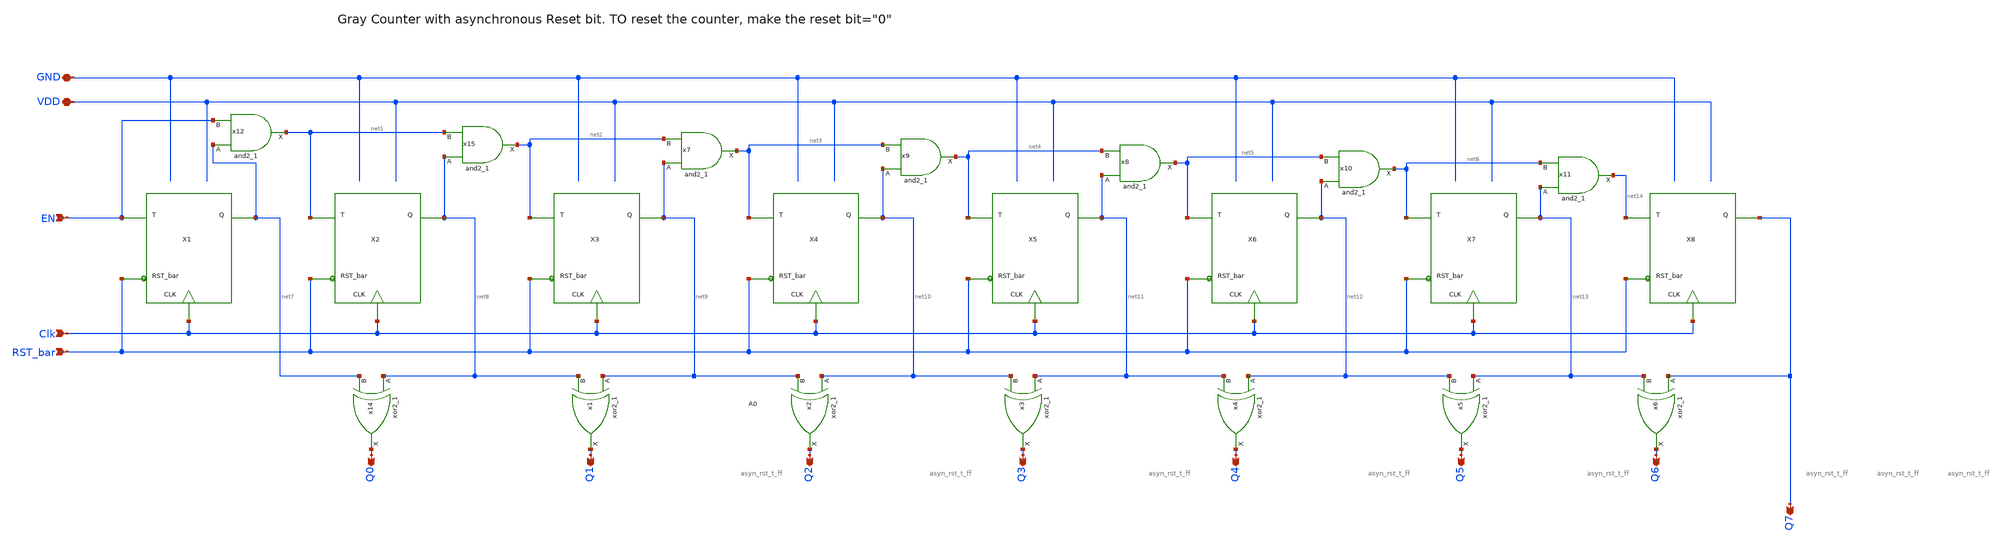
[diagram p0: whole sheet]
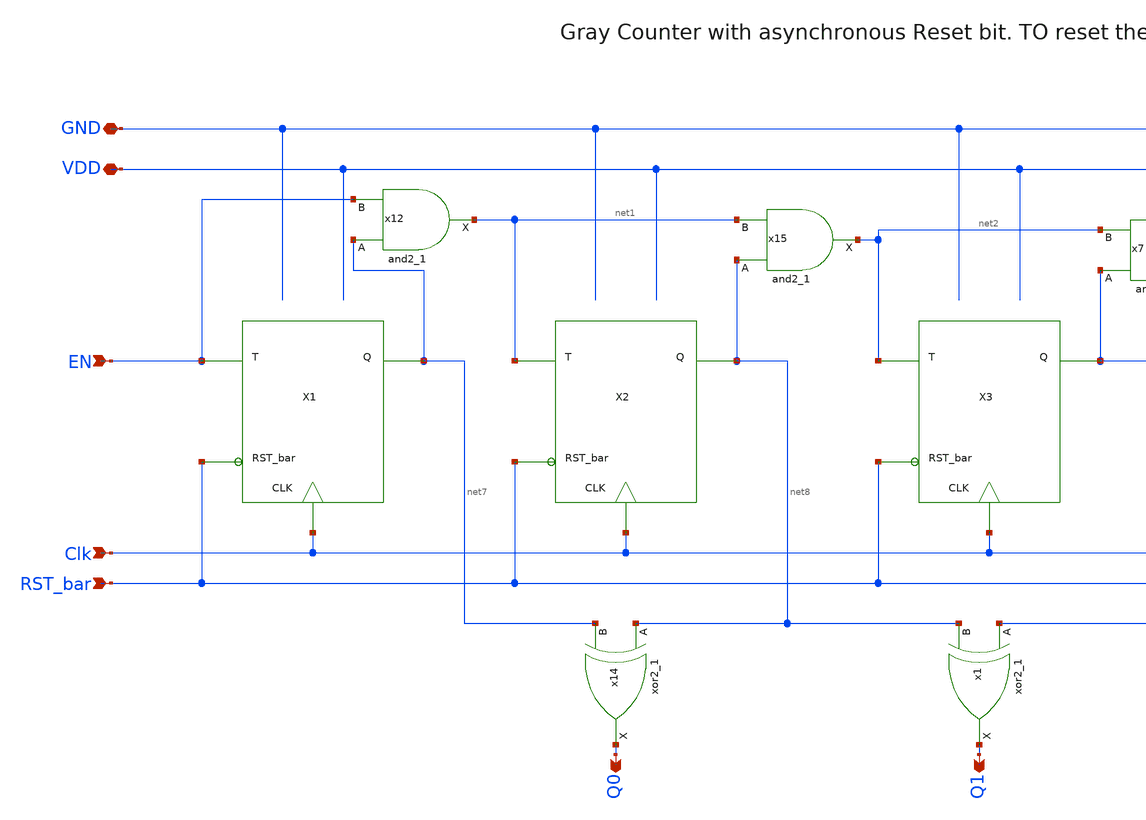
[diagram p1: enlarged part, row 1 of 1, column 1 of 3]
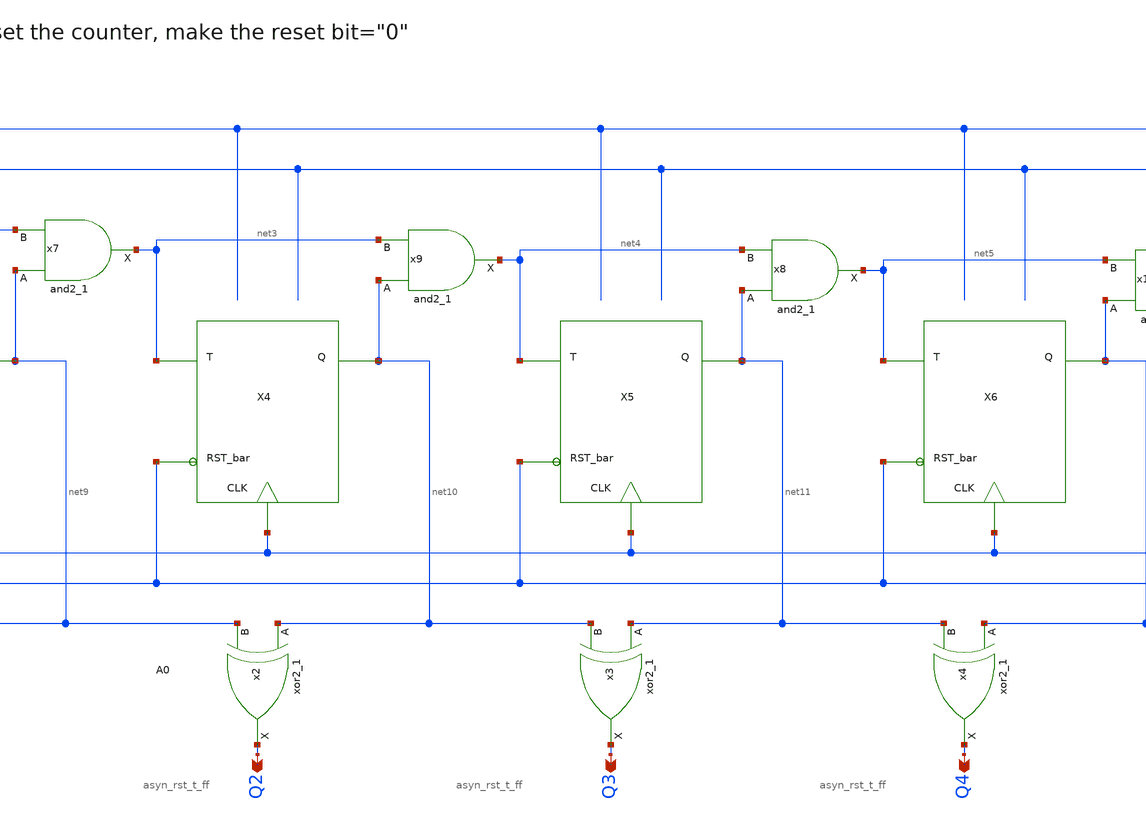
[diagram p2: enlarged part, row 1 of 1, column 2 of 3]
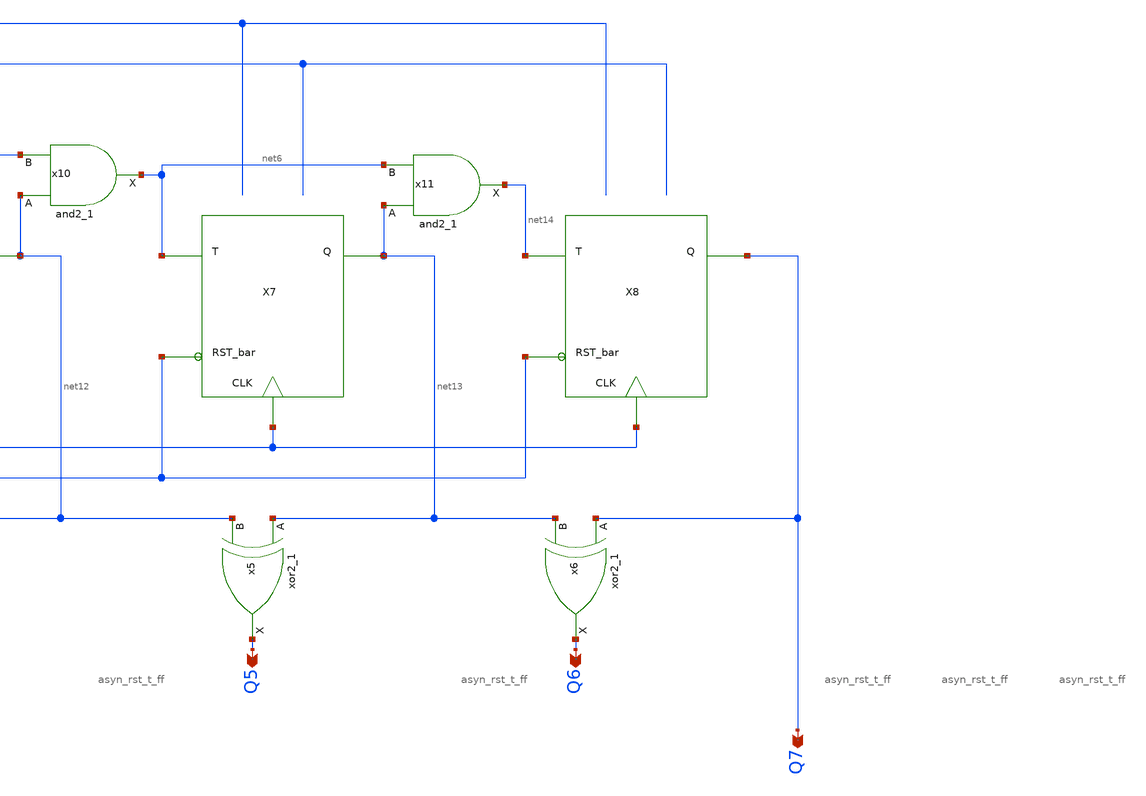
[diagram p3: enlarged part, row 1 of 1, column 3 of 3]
** sch_path: xschem/Asyn_rst_gray_counter/asyn_rst_gray_counter.sch
**.subckt asyn_rst_gray_counter Clk EN Q0 Q1 Q2 Q4 Q5 Q6 Q7 Q3 RST_bar VDD GND
*.ipin Clk
*.ipin EN
*.opin Q0
*.opin Q1
*.opin Q2
*.opin Q4
*.opin Q5
*.opin Q6
*.opin Q7
*.opin Q3
*.ipin RST_bar
*.iopin VDD
*.iopin GND
x14 net8 net7 GND GND VDD VDD Q0 sky130_fd_sc_lp__xor2_1
x15 net8 net1 GND GND VDD VDD net2 sky130_fd_sc_lp__and2_1
x1 net9 net8 GND GND VDD VDD Q1 sky130_fd_sc_lp__xor2_1
x2 net10 net9 GND GND VDD VDD Q2 sky130_fd_sc_lp__xor2_1
x3 net11 net10 GND GND VDD VDD Q3 sky130_fd_sc_lp__xor2_1
x4 net12 net11 GND GND VDD VDD Q4 sky130_fd_sc_lp__xor2_1
x5 net13 net12 GND GND VDD VDD Q5 sky130_fd_sc_lp__xor2_1
x6 Q7 net13 GND GND VDD VDD Q6 sky130_fd_sc_lp__xor2_1
x7 net9 net2 GND GND VDD VDD net3 sky130_fd_sc_lp__and2_1
x8 net11 net4 GND GND VDD VDD net5 sky130_fd_sc_lp__and2_1
x9 net10 net3 GND GND VDD VDD net4 sky130_fd_sc_lp__and2_1
x10 net12 net5 GND GND VDD VDD net6 sky130_fd_sc_lp__and2_1
x11 net13 net6 GND GND VDD VDD net14 sky130_fd_sc_lp__and2_1
x12 net7 EN GND GND VDD VDD net1 sky130_fd_sc_lp__and2_1
X1 EN net7 Clk RST_bar asyn_rst_t_ff
X2 net1 net8 Clk RST_bar asyn_rst_t_ff
X3 net2 net9 Clk RST_bar asyn_rst_t_ff
X4 net3 net10 Clk RST_bar asyn_rst_t_ff
X5 net4 net11 Clk RST_bar asyn_rst_t_ff
X6 net5 net12 Clk RST_bar asyn_rst_t_ff
X7 net6 net13 Clk RST_bar asyn_rst_t_ff
X8 net14 Q7 Clk RST_bar asyn_rst_t_ff
**.ends

* expanding   symbol:  T_flip_flop/asyn_rst_t_ff.sym # of pins=4
** sym_path: xschem/T_flip_flop/asyn_rst_t_ff.sym
** sch_path: xschem/T_flip_flop/asyn_rst_t_ff.sch
.subckt asyn_rst_t_ff T Q CLK RST_bar
*.ipin T
*.ipin CLK
*.opin Q
*.ipin RST_bar
x1 CLK net1 RST_bar GND GND VDD VDD Q sky130_fd_sc_lp__dfrtp_1
x3 T Q GND GND VDD VDD net1 sky130_fd_sc_lp__xor2_1
.ends

.end
